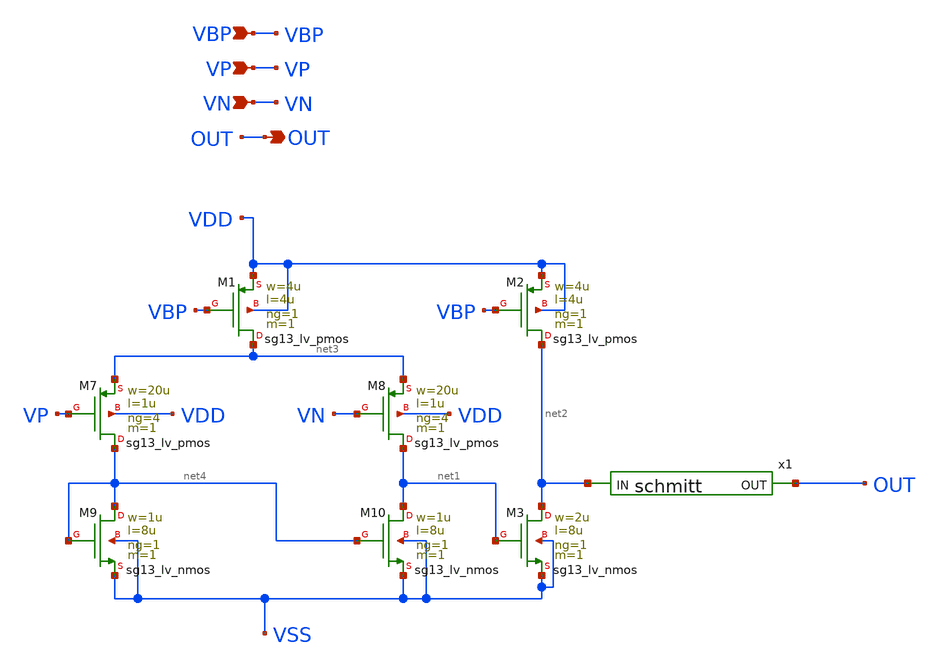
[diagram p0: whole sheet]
** sch_path: design/blocks/comparator/schematic/comp_inf.sch
**.subckt comp_inf OUT VN VP VBP
*.opin OUT
*.ipin VN
*.ipin VP
*.ipin VBP
XM1 net3 VBP VDD VDD sg13_lv_pmos w=4u l=4u ng=1 m=1 mm_ok=1
XM7 net4 VP net3 VDD sg13_lv_pmos w=20u l=1u ng=4 m=1 mm_ok=1
XM8 net1 VN net3 VDD sg13_lv_pmos w=20u l=1u ng=4 m=1 mm_ok=1
XM9 net4 net4 VSS VSS sg13_lv_nmos w=1u l=8u ng=1 m=1 mm_ok=1
XM10 net1 net4 VSS VSS sg13_lv_nmos w=1u l=8u ng=1 m=1 mm_ok=1
XM2 net2 VBP VDD VDD sg13_lv_pmos w=4u l=4u ng=1 m=1 mm_ok=1
XM3 net2 net1 VSS VSS sg13_lv_nmos w=2u l=8u ng=1 m=1 mm_ok=1
x1 net2 OUT VDD VSS schmitt
**.ends

* expanding   symbol:  schmitt.sym # of pins=2
** sym_path: design/blocks/schmitt/schematic/schmitt.sym
** sch_path: design/blocks/schmitt/schematic/schmitt.sch
.subckt schmitt IN OUT VDD VSS
*.opin OUT
*.ipin IN
XM4 net1 IN VDD VDD sg13_lv_pmos w=1.04u l=0.13u ng=1 m=1 mm_ok=1
XM6 OUT IN net2 VSS sg13_lv_nmos w=0.76u l=0.13u ng=1 m=1 mm_ok=1
XM5 OUT IN net1 VDD sg13_lv_pmos w=1.04u l=0.13u ng=1 m=1 mm_ok=1
XM7 net2 IN VSS VSS sg13_lv_nmos w=0.76u l=0.13u ng=1 m=1 mm_ok=1
XM8 VSS OUT net1 VDD sg13_lv_pmos w=0.42u l=0.13u ng=1 m=1 mm_ok=1
XM9 VDD OUT net2 VSS sg13_lv_nmos w=0.42u l=0.13u ng=1 m=1 mm_ok=1
.ends

.end
